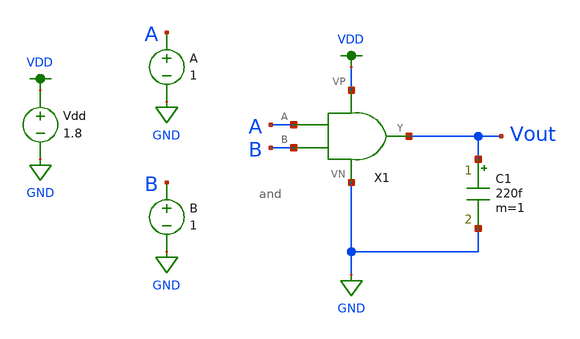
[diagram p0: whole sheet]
** sch_path: MP1/and_tran.sch
**.subckt and_tran
X1 A B Vout VDD GND and
C1 Vout GND 220f m=1
Vdd VDD GND 1.8
A A GND 1
B B GND 1
**** begin user architecture code

.option wnflag=1
.lib ~/skywater/skywater-pdk/libraries/sky130_fd_pr_ngspice/latest/models/sky130.lib.spice tt

**** end user architecture code
**.ends
.GLOBAL VDD
.GLOBAL GND
.end
